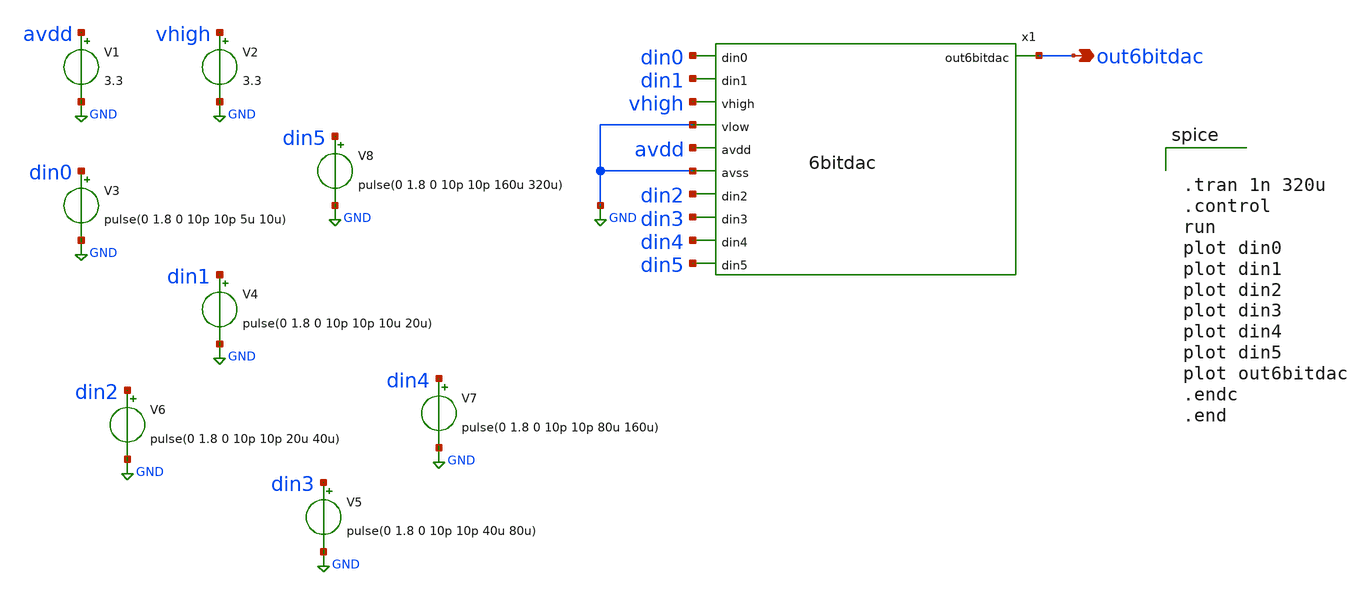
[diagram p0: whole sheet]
** sch_path: xschem/tb_6bitdac.sch
**.subckt tb_6bitdac out6bitdac
*.opin out6bitdac
x1 out6bitdac din0 din1 vhigh GND avdd GND din2 din3 din4 din5 6bitdac
V1 avdd GND 3.3
V2 vhigh GND 3.3
V3 din0 GND pulse(0 1.8 0 10p 10p 5u 10u)
V4 din1 GND pulse(0 1.8 0 10p 10p 10u 20u)
V6 din2 GND pulse(0 1.8 0 10p 10p 20u 40u)
V5 din3 GND pulse(0 1.8 0 10p 10p 40u 80u)
V7 din4 GND pulse(0 1.8 0 10p 10p 80u 160u)
V8 din5 GND pulse(0 1.8 0 10p 10p 160u 320u)
**** begin user architecture code

** opencircuitdesign pdks install
.lib $::SKYWATER_MODELS/sky130.lib.spice tt




.tran 1n 320u
.control
run
plot din0
plot din1
plot din2
plot din3
plot din4
plot din5
plot out6bitdac
.endc
.end

**** end user architecture code
**.ends
.GLOBAL GND
.end
